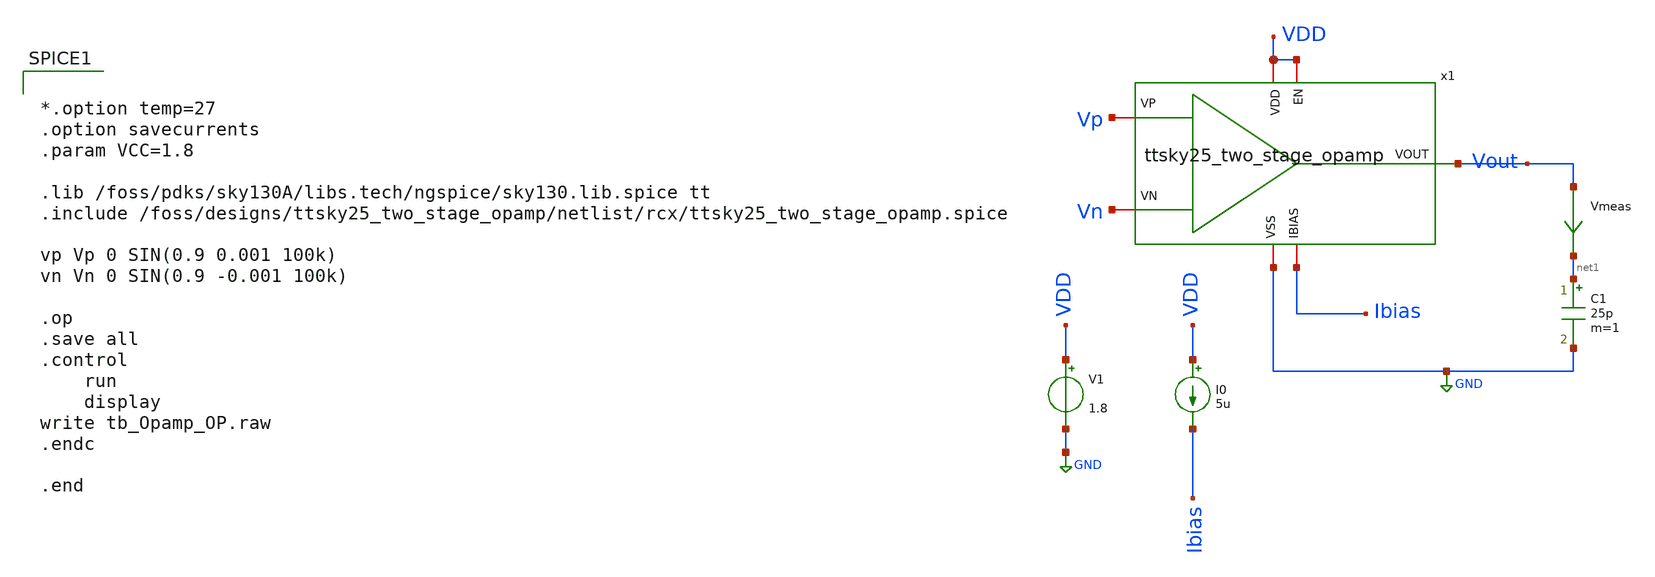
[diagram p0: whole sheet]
** sch_path: xschem/post-layout/testbenches/tb_Opamp_OP.sch
**.subckt tb_Opamp_OP
V1 VDD GND 1.8
I0 VDD Ibias 5u
C1 net1 GND 25p m=1
x1 VDD Ibias Vout Vn Vp VDD GND ttsky25_two_stage_opamp
Vmeas Vout net1 0
.save i(vmeas)
**** begin user architecture code


*.option temp=27
.option savecurrents
.param VCC=1.8

.lib /foss/pdks/sky130A/libs.tech/ngspice/sky130.lib.spice tt
.include /foss/designs/ttsky25_two_stage_opamp/netlist/rcx/ttsky25_two_stage_opamp.spice

vp Vp 0 SIN(0.9 0.001 100k)
vn Vn 0 SIN(0.9 -0.001 100k)

.op
.save all
.control
	run
	display
write tb_Opamp_OP.raw
.endc

.end


**** end user architecture code
**.ends
.GLOBAL GND
.end
